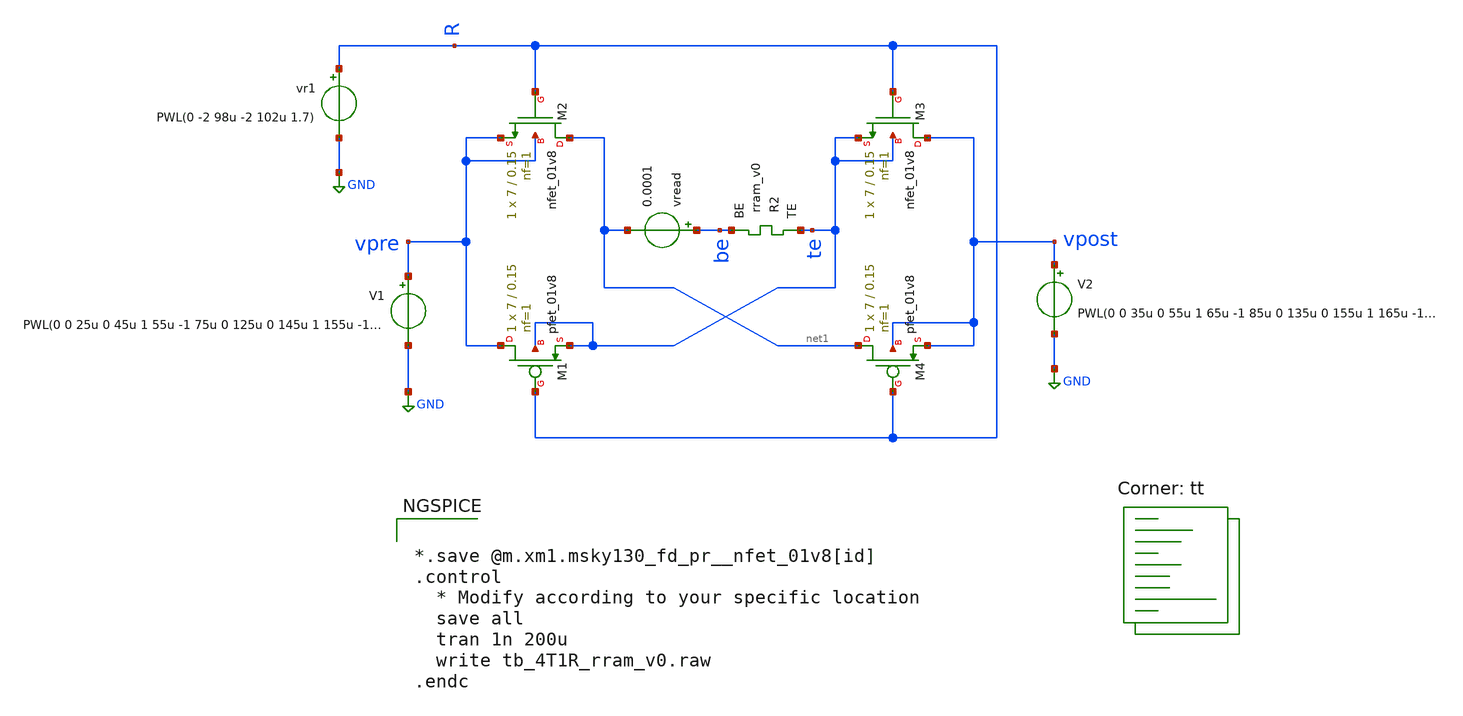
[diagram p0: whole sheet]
** sch_path: Synapse/tb_4T1R_rram_v0.sch
**.subckt tb_4T1R_rram_v0
XR2 te be rram_v0
XM2 net1 R vpre vpre sky130_fd_pr__nfet_01v8 L=0.15 W=7 nf=1 ad='int((nf+1)/2) * W/nf * 0.29' as='int((nf+2)/2) * W/nf * 0.29'
+ pd='2*int((nf+1)/2) * (W/nf + 0.29)' ps='2*int((nf+2)/2) * (W/nf + 0.29)' nrd='0.29 / W' nrs='0.29 / W'
+ sa=0 sb=0 sd=0 mult=1 m=1
XM3 vpost R te te sky130_fd_pr__nfet_01v8 L=0.15 W=7 nf=1 ad='int((nf+1)/2) * W/nf * 0.29' as='int((nf+2)/2) * W/nf * 0.29'
+ pd='2*int((nf+1)/2) * (W/nf + 0.29)' ps='2*int((nf+2)/2) * (W/nf + 0.29)' nrd='0.29 / W' nrs='0.29 / W'
+ sa=0 sb=0 sd=0 mult=1 m=1
V1 vpre GND PWL(0 0 25u 0 45u 1 55u -1 75u 0 125u 0 145u 1 155u -1 175u 0)
V2 vpost GND PWL(0 0 35u 0 55u 1 65u -1 85u 0 135u 0 155u 1 165u -1 185u 0)
vread be net1 0.0001
vr1 R GND PWL(0 -2 98u -2 102u 1.7)
XM1 vpre R te te sky130_fd_pr__pfet_01v8 L=0.15 W=7 nf=1 ad='int((nf+1)/2) * W/nf * 0.29' as='int((nf+2)/2) * W/nf * 0.29'
+ pd='2*int((nf+1)/2) * (W/nf + 0.29)' ps='2*int((nf+2)/2) * (W/nf + 0.29)' nrd='0.29 / W' nrs='0.29 / W'
+ sa=0 sb=0 sd=0 mult=1 m=1
XM4 net1 R vpost vpost sky130_fd_pr__pfet_01v8 L=0.15 W=7 nf=1 ad='int((nf+1)/2) * W/nf * 0.29' as='int((nf+2)/2) * W/nf * 0.29'
+ pd='2*int((nf+1)/2) * (W/nf + 0.29)' ps='2*int((nf+2)/2) * (W/nf + 0.29)' nrd='0.29 / W' nrs='0.29 / W'
+ sa=0 sb=0 sd=0 mult=1 m=1
**** begin user architecture code


*.save @m.xm1.msky130_fd_pr__nfet_01v8[id]
.control
  * Modify according to your specific location
  save all
  tran 1n 200u
  write tb_4T1R_rram_v0.raw
.endc



.lib $::SKYWATER_MODELS/sky130.lib.spice tt

** opencircuitdesign pdks install
.inc $::SKYWATER_MODELS/rram_v0.spice

**** end user architecture code
**.ends
.GLOBAL GND
.end
